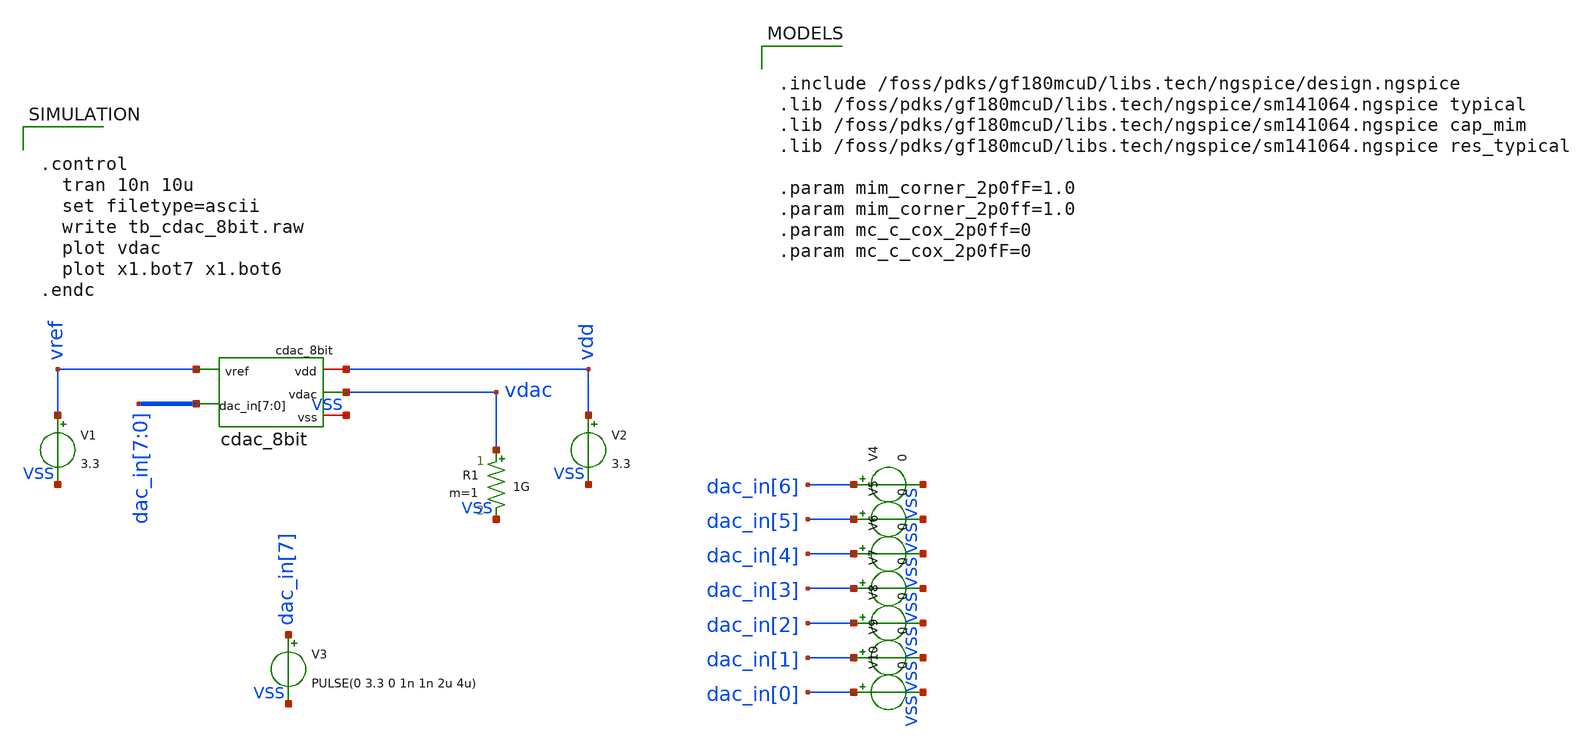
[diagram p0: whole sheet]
** sch_path: xschem/sar_adc/blocks/cdac/testbench/tb_cdac_8bit.sch
**.subckt tb_cdac_8bit
V1 vref VSS 3.3
V2 vdd VSS 3.3
R1 vdac VSS 1G m=1
V3 dac_in[7] VSS PULSE(0 3.3 0 1n 1n 2u 4u)
V4 dac_in[6] VSS 0
V5 dac_in[5] VSS 0
V6 dac_in[4] VSS 0
V7 dac_in[3] VSS 0
V8 dac_in[2] VSS 0
V9 dac_in[1] VSS 0
V10 dac_in[0] VSS 0
x1 vref vdd VSS dac_in[7] dac_in[6] dac_in[5] dac_in[4] dac_in[3] dac_in[2] dac_in[1] dac_in[0] vdac
+ cdac_8bit
**** begin user architecture code


.include /foss/pdks/gf180mcuD/libs.tech/ngspice/design.ngspice
.lib /foss/pdks/gf180mcuD/libs.tech/ngspice/sm141064.ngspice typical
.lib /foss/pdks/gf180mcuD/libs.tech/ngspice/sm141064.ngspice cap_mim
.lib /foss/pdks/gf180mcuD/libs.tech/ngspice/sm141064.ngspice res_typical

.param mim_corner_2p0fF=1.0
.param mim_corner_2p0ff=1.0
.param mc_c_cox_2p0ff=0
.param mc_c_cox_2p0fF=0




.control
  tran 10n 10u
  set filetype=ascii
  write tb_cdac_8bit.raw
  plot vdac
  plot x1.bot7 x1.bot6
.endc


**** end user architecture code
**.ends
.end
